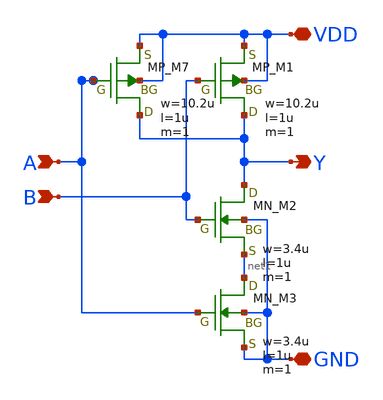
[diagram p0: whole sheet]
** sch_path: libs.tech/xschem/TR-1um_stdcell/NAND2.sch
**.subckt NAND2 B A Y GND VDD
*.ipin B
*.ipin A
*.opin Y
*.iopin GND
*.iopin VDD
XM7 Y A VDD VDD PMOS w=10.2u l=1u nrd=0 nrs=0 m=1
XM1 Y B VDD VDD PMOS w=10.2u l=1u nrd=0 nrs=0 m=1
XM2 Y B net1 GND NMOS w=3.4u l=1u nrd=0 nrs=0 m=1
XM3 net1 A GND GND NMOS w=3.4u l=1u nrd=0 nrs=0 m=1
**.ends
.end
